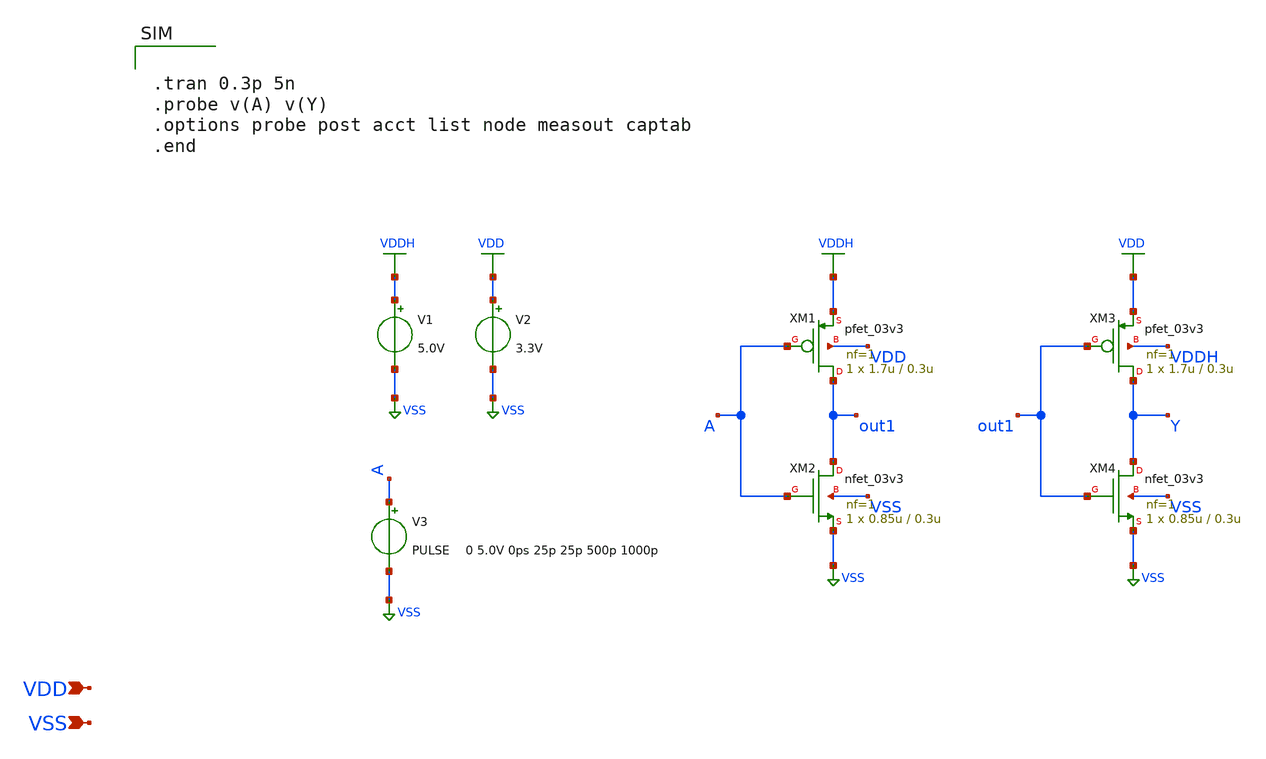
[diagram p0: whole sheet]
** sch_path: gf180mcu_osu_sc_gp9t3v3/xschem/gf180mcu_osu_sc_gp9t3v3__lshifdown.sch
**.subckt gf180mcu_osu_sc_gp9t3v3__lshifdown VDD VSS
*.ipin VDD
*.ipin VSS
XM1 out1 A VDDH VDD pfet_03v3 L=0.3u W=1.7u nf=1 ad='int((nf+1)/2) * W/nf * 0.18u' as='int((nf+2)/2) * W/nf * 0.18u'
+ pd='2*int((nf+1)/2) * (W/nf + 0.18u)' ps='2*int((nf+2)/2) * (W/nf + 0.18u)' nrd='0.18u / W' nrs='0.18u / W'
+ sa=0 sb=0 sd=0 m=1
XM2 out1 A VSS VSS nfet_03v3 L=0.3u W=0.85u nf=1 ad='int((nf+1)/2) * W/nf * 0.18u' as='int((nf+2)/2) * W/nf * 0.18u'
+ pd='2*int((nf+1)/2) * (W/nf + 0.18u)' ps='2*int((nf+2)/2) * (W/nf + 0.18u)' nrd='0.18u / W' nrs='0.18u / W'
+ sa=0 sb=0 sd=0 m=1
XM3 Y out1 VDD VDDH pfet_03v3 L=0.3u W=1.7u nf=1 ad='int((nf+1)/2) * W/nf * 0.18u' as='int((nf+2)/2) * W/nf * 0.18u'
+ pd='2*int((nf+1)/2) * (W/nf + 0.18u)' ps='2*int((nf+2)/2) * (W/nf + 0.18u)' nrd='0.18u / W' nrs='0.18u / W'
+ sa=0 sb=0 sd=0 m=1
XM4 Y out1 VSS VSS nfet_03v3 L=0.3u W=0.85u nf=1 ad='int((nf+1)/2) * W/nf * 0.18u' as='int((nf+2)/2) * W/nf * 0.18u'
+ pd='2*int((nf+1)/2) * (W/nf + 0.18u)' ps='2*int((nf+2)/2) * (W/nf + 0.18u)' nrd='0.18u / W' nrs='0.18u / W'
+ sa=0 sb=0 sd=0 m=1
V1 VDDH VSS 5.0V
V2 VDD VSS 3.3V
V3 A VSS PULSE 0 5.0V 0ps 25p 25p 500p 1000p
**** begin user architecture code

.temp 25
.inc "/import/yukari1/lrburle/OSU_180/char/techfiles/design.hspice"
.lib "/import/yukari1/lrburle/OSU_180/char/techfiles/sm141064.hspice" typical



.tran 0.3p 5n
.probe v(A) v(Y)
.options probe post acct list node measout captab
.end


**** end user architecture code
**.ends
.GLOBAL VDDH
.GLOBAL VSS
.GLOBAL VDD
.end
